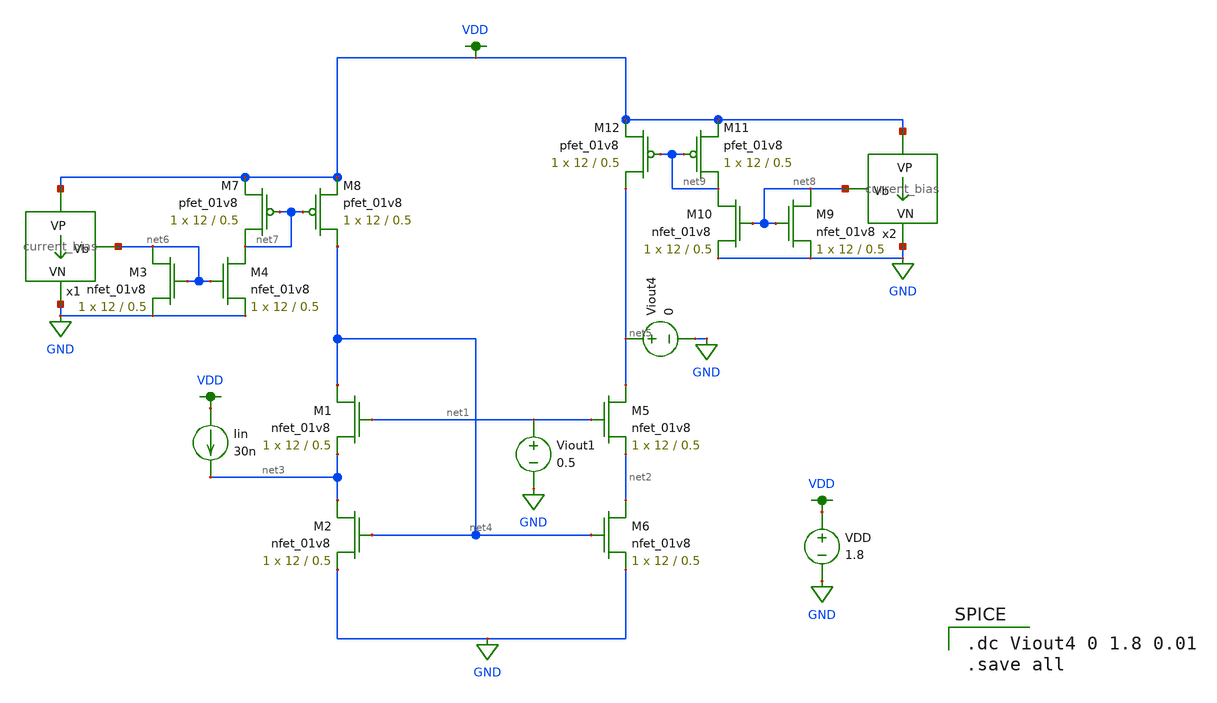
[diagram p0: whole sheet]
** sch_path: schematics/current mirrors/FVF_current_mirror_3.sch
**.subckt FVF_current_mirror_3
XM1 net4 net1 net3 GND sky130_fd_pr__nfet_01v8 L=0.5 W=12 nf=1 ad='int((nf+1)/2) * W/nf * 0.29' as='int((nf+2)/2) * W/nf * 0.29'
+ pd='2*int((nf+1)/2) * (W/nf + 0.29)' ps='2*int((nf+2)/2) * (W/nf + 0.29)' nrd='0.29 / W' nrs='0.29 / W'
+ sa=0 sb=0 sd=0 mult=1 m=1
XM2 net3 net4 GND GND sky130_fd_pr__nfet_01v8 L=0.5 W=12 nf=1 ad='int((nf+1)/2) * W/nf * 0.29' as='int((nf+2)/2) * W/nf * 0.29'
+ pd='2*int((nf+1)/2) * (W/nf + 0.29)' ps='2*int((nf+2)/2) * (W/nf + 0.29)' nrd='0.29 / W' nrs='0.29 / W'
+ sa=0 sb=0 sd=0 mult=1 m=1
XM5 net5 net1 net2 GND sky130_fd_pr__nfet_01v8 L=0.5 W=12 nf=1 ad='int((nf+1)/2) * W/nf * 0.29' as='int((nf+2)/2) * W/nf * 0.29'
+ pd='2*int((nf+1)/2) * (W/nf + 0.29)' ps='2*int((nf+2)/2) * (W/nf + 0.29)' nrd='0.29 / W' nrs='0.29 / W'
+ sa=0 sb=0 sd=0 mult=1 m=1
XM6 net2 net4 GND GND sky130_fd_pr__nfet_01v8 L=0.5 W=12 nf=1 ad='int((nf+1)/2) * W/nf * 0.29' as='int((nf+2)/2) * W/nf * 0.29'
+ pd='2*int((nf+1)/2) * (W/nf + 0.29)' ps='2*int((nf+2)/2) * (W/nf + 0.29)' nrd='0.29 / W' nrs='0.29 / W'
+ sa=0 sb=0 sd=0 mult=1 m=1
Viout4 net5 GND 0
Iin VDD net3 30n
VDD VDD GND 1.8
x1 VDD net6 GND current_bias
XM3 net6 net6 GND GND sky130_fd_pr__nfet_01v8 L=0.5 W=12 nf=1 ad='int((nf+1)/2) * W/nf * 0.29' as='int((nf+2)/2) * W/nf * 0.29'
+ pd='2*int((nf+1)/2) * (W/nf + 0.29)' ps='2*int((nf+2)/2) * (W/nf + 0.29)' nrd='0.29 / W' nrs='0.29 / W'
+ sa=0 sb=0 sd=0 mult=1 m=1
XM4 net7 net6 GND GND sky130_fd_pr__nfet_01v8 L=0.5 W=12 nf=1 ad='int((nf+1)/2) * W/nf * 0.29' as='int((nf+2)/2) * W/nf * 0.29'
+ pd='2*int((nf+1)/2) * (W/nf + 0.29)' ps='2*int((nf+2)/2) * (W/nf + 0.29)' nrd='0.29 / W' nrs='0.29 / W'
+ sa=0 sb=0 sd=0 mult=1 m=1
XM7 net7 net7 VDD VDD sky130_fd_pr__pfet_01v8 L=0.5 W=12 nf=1 ad='int((nf+1)/2) * W/nf * 0.29' as='int((nf+2)/2) * W/nf * 0.29'
+ pd='2*int((nf+1)/2) * (W/nf + 0.29)' ps='2*int((nf+2)/2) * (W/nf + 0.29)' nrd='0.29 / W' nrs='0.29 / W'
+ sa=0 sb=0 sd=0 mult=1 m=1
x2 VDD net8 GND current_bias
XM9 net8 net8 GND GND sky130_fd_pr__nfet_01v8 L=0.5 W=12 nf=1 ad='int((nf+1)/2) * W/nf * 0.29' as='int((nf+2)/2) * W/nf * 0.29'
+ pd='2*int((nf+1)/2) * (W/nf + 0.29)' ps='2*int((nf+2)/2) * (W/nf + 0.29)' nrd='0.29 / W' nrs='0.29 / W'
+ sa=0 sb=0 sd=0 mult=1 m=1
XM10 net9 net8 GND GND sky130_fd_pr__nfet_01v8 L=0.5 W=12 nf=1 ad='int((nf+1)/2) * W/nf * 0.29' as='int((nf+2)/2) * W/nf * 0.29'
+ pd='2*int((nf+1)/2) * (W/nf + 0.29)' ps='2*int((nf+2)/2) * (W/nf + 0.29)' nrd='0.29 / W' nrs='0.29 / W'
+ sa=0 sb=0 sd=0 mult=1 m=1
XM8 net4 net7 VDD VDD sky130_fd_pr__pfet_01v8 L=0.5 W=12 nf=1 ad='int((nf+1)/2) * W/nf * 0.29' as='int((nf+2)/2) * W/nf * 0.29'
+ pd='2*int((nf+1)/2) * (W/nf + 0.29)' ps='2*int((nf+2)/2) * (W/nf + 0.29)' nrd='0.29 / W' nrs='0.29 / W'
+ sa=0 sb=0 sd=0 mult=1 m=1
XM12 net5 net9 VDD VDD sky130_fd_pr__pfet_01v8 L=0.5 W=12 nf=1 ad='int((nf+1)/2) * W/nf * 0.29' as='int((nf+2)/2) * W/nf * 0.29'
+ pd='2*int((nf+1)/2) * (W/nf + 0.29)' ps='2*int((nf+2)/2) * (W/nf + 0.29)' nrd='0.29 / W' nrs='0.29 / W'
+ sa=0 sb=0 sd=0 mult=1 m=1
XM11 net9 net9 VDD VDD sky130_fd_pr__pfet_01v8 L=0.5 W=12 nf=1 ad='int((nf+1)/2) * W/nf * 0.29' as='int((nf+2)/2) * W/nf * 0.29'
+ pd='2*int((nf+1)/2) * (W/nf + 0.29)' ps='2*int((nf+2)/2) * (W/nf + 0.29)' nrd='0.29 / W' nrs='0.29 / W'
+ sa=0 sb=0 sd=0 mult=1 m=1
Viout1 net1 GND 0.5
**** begin user architecture code

.option wnflag=1
.param MC_SWITCH=0.0
.lib ~/skywater/skywater-pdk/libraries/sky130_fd_pr_ngspice/latest/models/sky130.lib.spice tt


.dc Viout4 0 1.8 0.01
.save all

**** end user architecture code
**.ends
.GLOBAL GND
.GLOBAL VDD
.end
